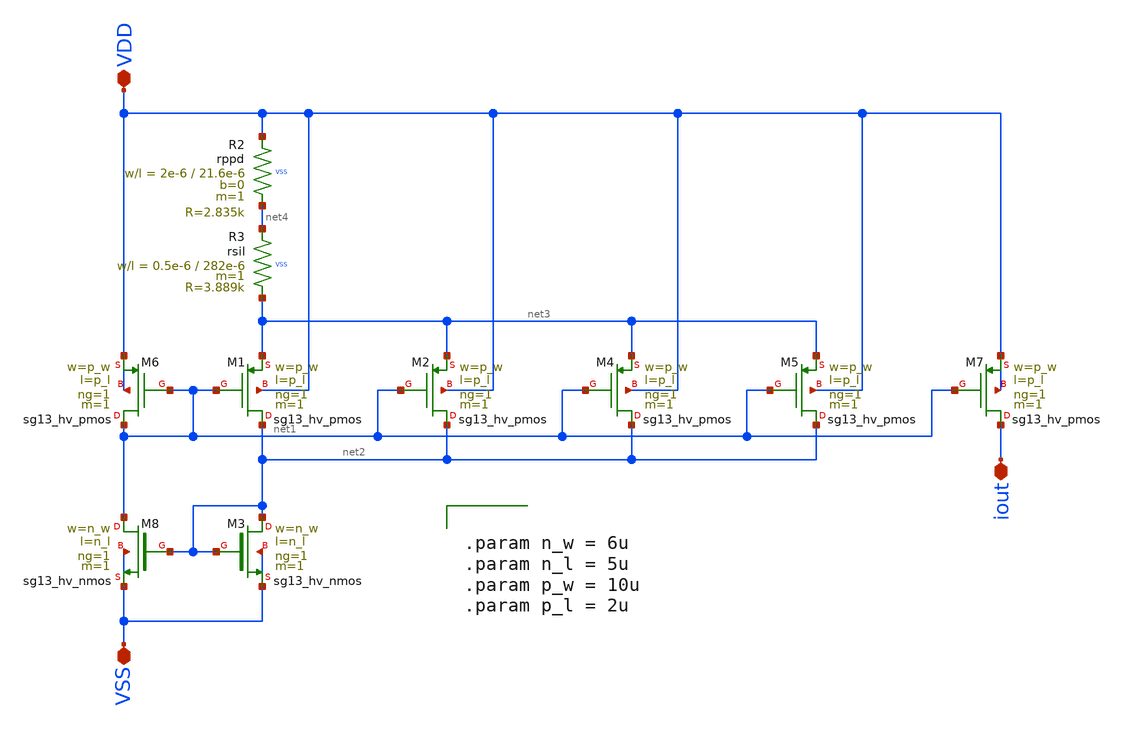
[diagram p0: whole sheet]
** sch_path: macros/heichips26_vcr/macros/switched_capacitor/schematic/xschem/current_reference_pmos_40uA.sch
**.subckt current_reference_pmos_40uA VSS VDD iout
*.iopin VSS
*.iopin VDD
*.iopin iout
XM8 net1 net2 VSS VSS sg13_hv_nmos w=n_w l=n_l ng=1 m=1 mm_ok=1
XM6 net1 net1 VDD VDD sg13_hv_pmos w=p_w l=p_l ng=1 m=1 mm_ok=1
XM1 net2 net1 net3 VDD sg13_hv_pmos w=p_w l=p_l ng=1 m=1 mm_ok=1
XM3 net2 net2 VSS VSS sg13_hv_nmos w=n_w l=n_l ng=1 m=1 mm_ok=1
XR2 VDD net4 VSS rppd w=2e-6 l=21.6e-6 m=1 b=0 mm_ok=1
XR3 net4 net3 VSS rsil w=0.5e-6 l=282e-6 m=1 mm_ok=1
XM2 net2 net1 net3 VDD sg13_hv_pmos w=p_w l=p_l ng=1 m=1 mm_ok=1
XM4 net2 net1 net3 VDD sg13_hv_pmos w=p_w l=p_l ng=1 m=1 mm_ok=1
XM5 net2 net1 net3 VDD sg13_hv_pmos w=p_w l=p_l ng=1 m=1 mm_ok=1
XM7 iout net1 VDD VDD sg13_hv_pmos w=p_w l=p_l ng=1 m=1 mm_ok=1
**** begin user architecture code


.param n_w = 6u
.param n_l = 5u
.param p_w = 10u
.param p_l = 2u


**** end user architecture code
**.ends
.end
